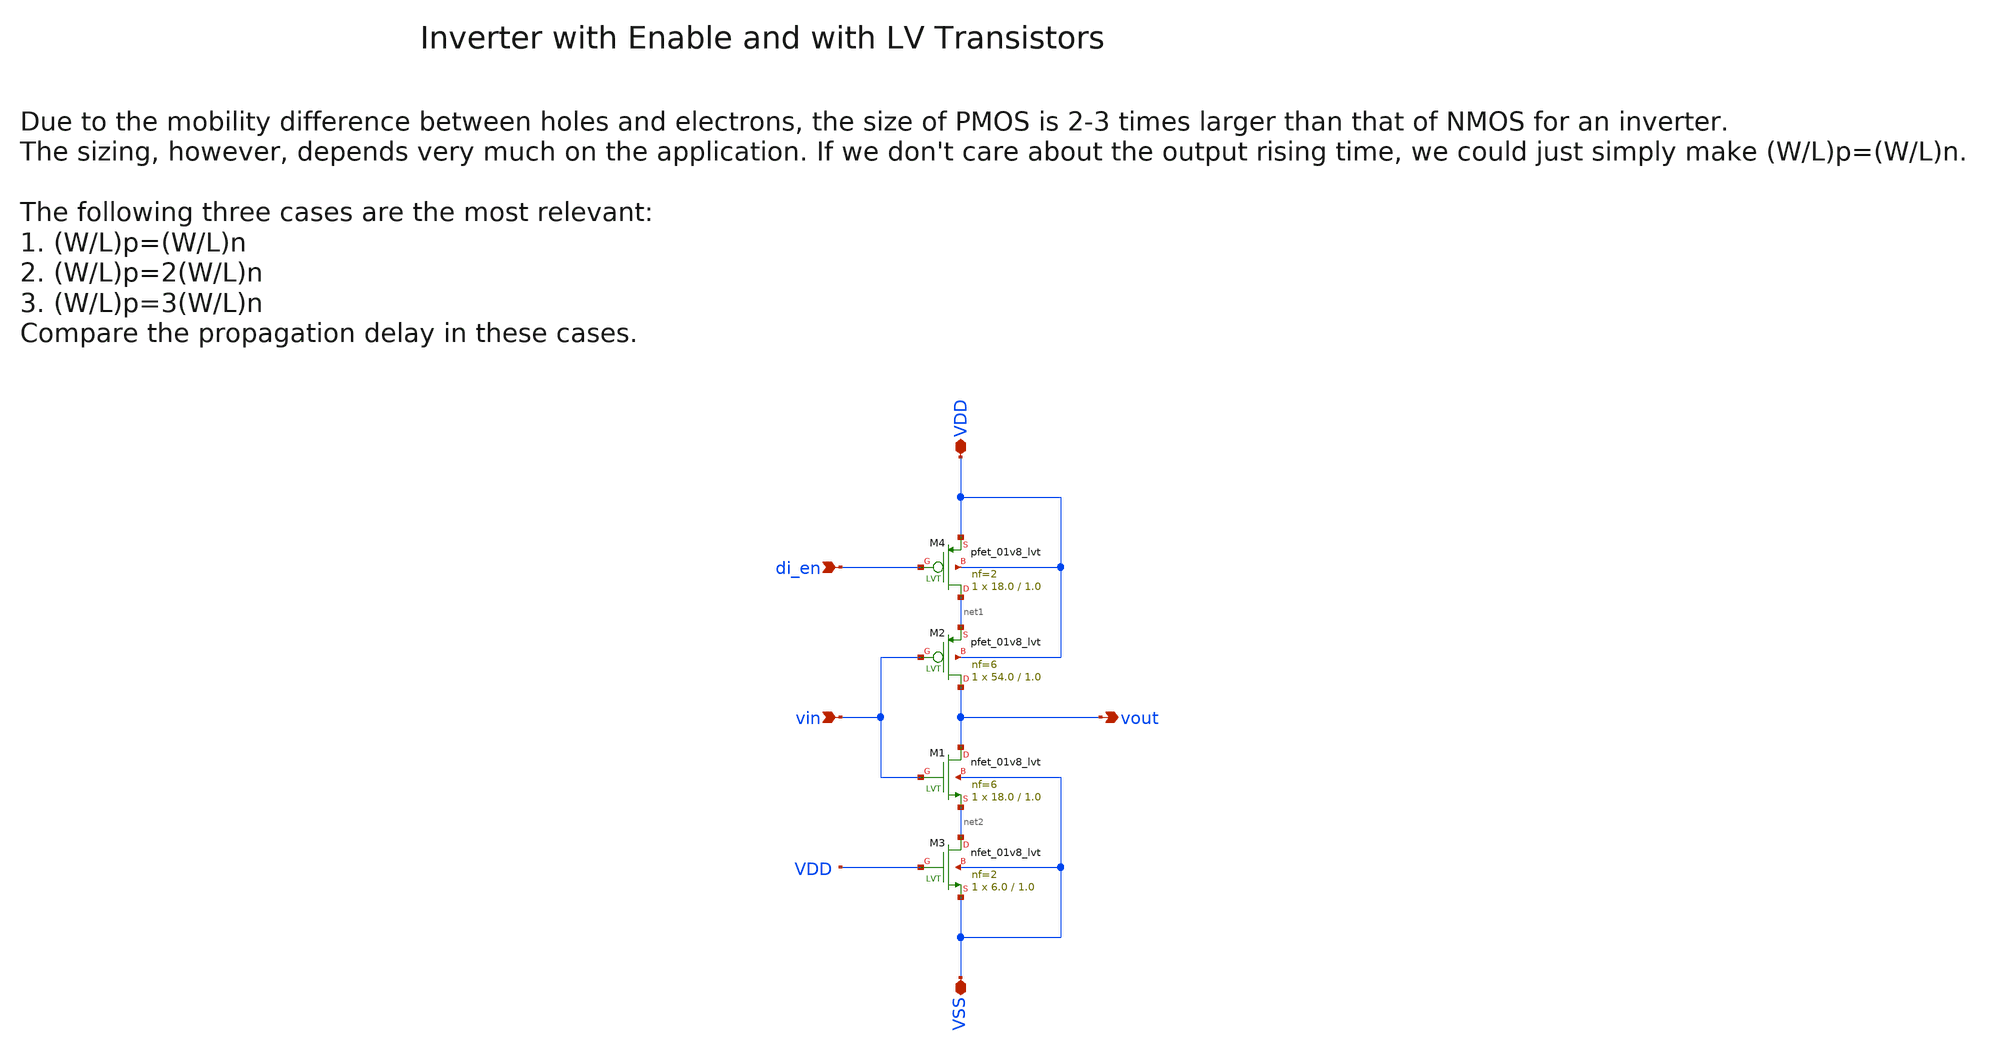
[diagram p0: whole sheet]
** sch_path: sky130/xschem/wspr_tx_iqmod_mfb_lpf_ota_core_inv_lv_en_NF6.sch
**.subckt wspr_tx_iqmod_mfb_lpf_ota_core_inv_lv_en_NF6 vin VDD VSS vout di_en
*.ipin vin
*.iopin VDD
*.iopin VSS
*.opin vout
*.ipin di_en
XM2 vout vin net1 VDD sky130_fd_pr__pfet_01v8_lvt L=1.0 W=54.0 nf=6 ad='int((6 + 1)/2) * 54.0 / 6 * 0.29'
+ as='int((6 + 2)/2) * 54.0 / 6 * 0.29' pd='2*int((6 + 1)/2) * (54.0 / 6 + 0.29)' ps='2*int((6 + 2)/2) * (54.0 / 6 + 0.29)'
+ nrd='0.29 / 54.0 ' nrs='0.29 / 54.0 ' sa=0 sb=0 sd=0 mult=1 m=1
XM3 net2 VDD VSS VSS sky130_fd_pr__nfet_01v8_lvt L=1.0 W=6.0 nf=2 ad='int((2 + 1)/2) * 6.0 / 2 * 0.29'
+ as='int((2 + 2)/2) * 6.0 / 2 * 0.29' pd='2*int((2 + 1)/2) * (6.0 / 2 + 0.29)' ps='2*int((2 + 2)/2) * (6.0 / 2 + 0.29)'
+ nrd='0.29 / 6.0 ' nrs='0.29 / 6.0 ' sa=0 sb=0 sd=0 mult=1 m=1
XM4 net1 di_en VDD VDD sky130_fd_pr__pfet_01v8_lvt L=1.0 W=18.0 nf=2 ad='int((2 + 1)/2) * 18.0 / 2 * 0.29'
+ as='int((2 + 2)/2) * 18.0 / 2 * 0.29' pd='2*int((2 + 1)/2) * (18.0 / 2 + 0.29)' ps='2*int((2 + 2)/2) * (18.0 / 2 + 0.29)'
+ nrd='0.29 / 18.0 ' nrs='0.29 / 18.0 ' sa=0 sb=0 sd=0 mult=1 m=1
XM1 vout vin net2 VSS sky130_fd_pr__nfet_01v8_lvt L=1.0 W=18.0 nf=6 ad='int((6 + 1)/2) * 18.0 / 6 * 0.29'
+ as='int((6 + 2)/2) * 18.0 / 6 * 0.29' pd='2*int((6 + 1)/2) * (18.0 / 6 + 0.29)' ps='2*int((6 + 2)/2) * (18.0 / 6 + 0.29)'
+ nrd='0.29 / 18.0 ' nrs='0.29 / 18.0 ' sa=0 sb=0 sd=0 mult=1 m=1
**.ends
.end
